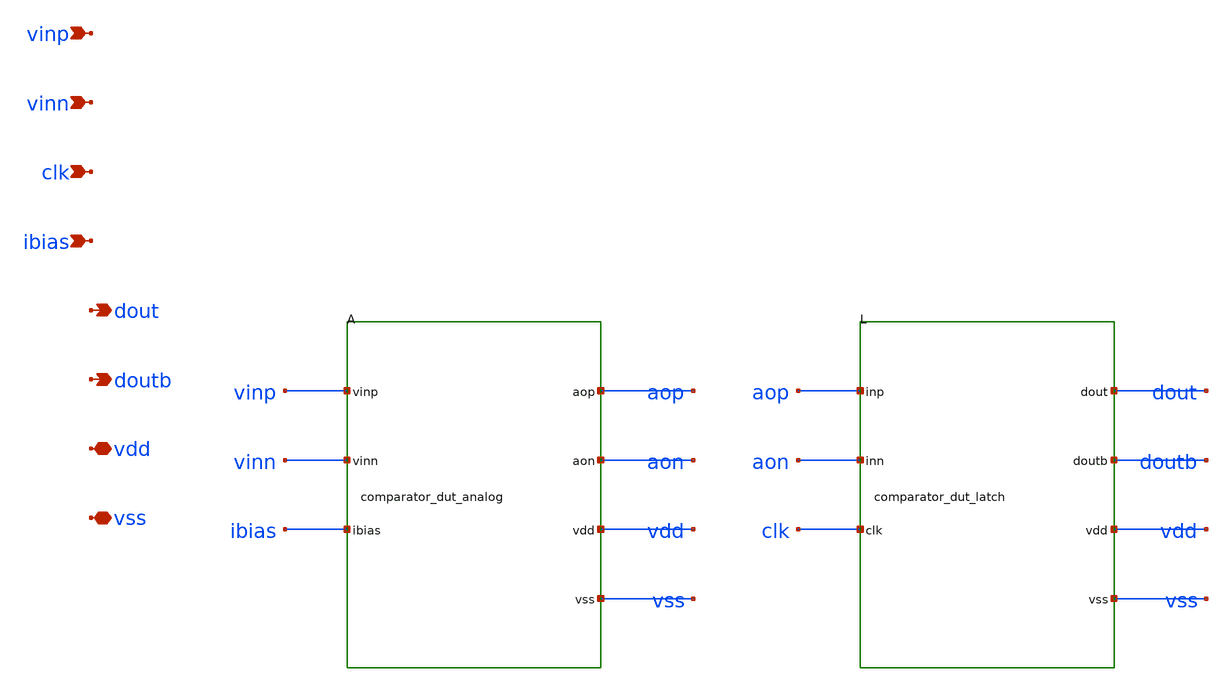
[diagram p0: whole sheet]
** sch_path: design/comparator_dut.sch
**.subckt comparator_dut vinp vinn clk ibias dout doutb vdd vss
*.ipin vinp
*.ipin vinn
*.ipin clk
*.ipin ibias
*.opin dout
*.opin doutb
*.iopin vdd
*.iopin vss
XA vinp vinn ibias aop aon vdd vss comparator_dut_analog
XL aop aon clk dout doutb vdd vss comparator_dut_latch
**.ends

* expanding   symbol:  comparator_dut_analog.sym # of pins=7
** sym_path: design/comparator_dut_analog.sym
** sch_path: design/comparator_dut_analog.sch
.subckt comparator_dut_analog vinp vinn ibias aop aon vdd vss

*.ipin vinp
*.ipin vinn
*.ipin ibias
*.opin aop
*.opin aon
*.iopin vdd
*.iopin vss
XMB ibias ibias vss vss nfet_03v3 L=4u W=5u nf=1 ad='int((nf+1)/2) * W/nf * 0.18u' as='int((nf+2)/2) * W/nf * 0.18u'
+ pd='2*int((nf+1)/2) * (W/nf + 0.18u)' ps='2*int((nf+2)/2) * (W/nf + 0.18u)' nrd='0.18u / W' nrs='0.18u / W'
+ sa=0 sb=0 sd=0 m=1
XMT atail ibias vss vss nfet_03v3 L=4u W=10u nf=1 ad='int((nf+1)/2) * W/nf * 0.18u' as='int((nf+2)/2) * W/nf * 0.18u'
+ pd='2*int((nf+1)/2) * (W/nf + 0.18u)' ps='2*int((nf+2)/2) * (W/nf + 0.18u)' nrd='0.18u / W' nrs='0.18u / W'
+ sa=0 sb=0 sd=0 m=1
XMIP aon vinp atail vss nfet_03v3 L=2u W=30u nf=1 ad='int((nf+1)/2) * W/nf * 0.18u' as='int((nf+2)/2) * W/nf * 0.18u'
+ pd='2*int((nf+1)/2) * (W/nf + 0.18u)' ps='2*int((nf+2)/2) * (W/nf + 0.18u)' nrd='0.18u / W' nrs='0.18u / W'
+ sa=0 sb=0 sd=0 m=1
XMIN aop vinn atail vss nfet_03v3 L=2u W=30u nf=1 ad='int((nf+1)/2) * W/nf * 0.18u' as='int((nf+2)/2) * W/nf * 0.18u'
+ pd='2*int((nf+1)/2) * (W/nf + 0.18u)' ps='2*int((nf+2)/2) * (W/nf + 0.18u)' nrd='0.18u / W' nrs='0.18u / W'
+ sa=0 sb=0 sd=0 m=1
XRN aon vdd vss ppolyf_u_1k r_width=1u r_length=120u m=1
XRP aop vdd vss ppolyf_u_1k r_width=1u r_length=120u m=1
.ends


* expanding   symbol:  comparator_dut_latch.sym # of pins=7
** sym_path: design/comparator_dut_latch.sym
** sch_path: design/comparator_dut_latch.sch
.subckt comparator_dut_latch inp inn clk dout doutb vdd vss

*.ipin inp
*.ipin inn
*.ipin clk
*.opin dout
*.opin doutb
*.iopin vdd
*.iopin vss
XMTL ltail clk vss vss nfet_03v3 L=0.5u W=16u nf=1 ad='int((nf+1)/2) * W/nf * 0.18u' as='int((nf+2)/2) * W/nf * 0.18u'
+ pd='2*int((nf+1)/2) * (W/nf + 0.18u)' ps='2*int((nf+2)/2) * (W/nf + 0.18u)' nrd='0.18u / W' nrs='0.18u / W'
+ sa=0 sb=0 sd=0 m=1
XM1 mn inp ltail vss nfet_03v3 L=0.5u W=8u nf=1 ad='int((nf+1)/2) * W/nf * 0.18u' as='int((nf+2)/2) * W/nf * 0.18u'
+ pd='2*int((nf+1)/2) * (W/nf + 0.18u)' ps='2*int((nf+2)/2) * (W/nf + 0.18u)' nrd='0.18u / W' nrs='0.18u / W'
+ sa=0 sb=0 sd=0 m=1
XM2 mp inn ltail vss nfet_03v3 L=0.5u W=8u nf=1 ad='int((nf+1)/2) * W/nf * 0.18u' as='int((nf+2)/2) * W/nf * 0.18u'
+ pd='2*int((nf+1)/2) * (W/nf + 0.18u)' ps='2*int((nf+2)/2) * (W/nf + 0.18u)' nrd='0.18u / W' nrs='0.18u / W'
+ sa=0 sb=0 sd=0 m=1
XM3 qn qp mn vss nfet_03v3 L=0.5u W=6u nf=1 ad='int((nf+1)/2) * W/nf * 0.18u' as='int((nf+2)/2) * W/nf * 0.18u'
+ pd='2*int((nf+1)/2) * (W/nf + 0.18u)' ps='2*int((nf+2)/2) * (W/nf + 0.18u)' nrd='0.18u / W' nrs='0.18u / W'
+ sa=0 sb=0 sd=0 m=1
XM4 qp qn mp vss nfet_03v3 L=0.5u W=6u nf=1 ad='int((nf+1)/2) * W/nf * 0.18u' as='int((nf+2)/2) * W/nf * 0.18u'
+ pd='2*int((nf+1)/2) * (W/nf + 0.18u)' ps='2*int((nf+2)/2) * (W/nf + 0.18u)' nrd='0.18u / W' nrs='0.18u / W'
+ sa=0 sb=0 sd=0 m=1
XM5 qn qp vdd vdd pfet_03v3 L=0.5u W=6u nf=1 ad='int((nf+1)/2) * W/nf * 0.18u' as='int((nf+2)/2) * W/nf * 0.18u'
+ pd='2*int((nf+1)/2) * (W/nf + 0.18u)' ps='2*int((nf+2)/2) * (W/nf + 0.18u)' nrd='0.18u / W' nrs='0.18u / W'
+ sa=0 sb=0 sd=0 m=1
XM6 qp qn vdd vdd pfet_03v3 L=0.5u W=6u nf=1 ad='int((nf+1)/2) * W/nf * 0.18u' as='int((nf+2)/2) * W/nf * 0.18u'
+ pd='2*int((nf+1)/2) * (W/nf + 0.18u)' ps='2*int((nf+2)/2) * (W/nf + 0.18u)' nrd='0.18u / W' nrs='0.18u / W'
+ sa=0 sb=0 sd=0 m=1
XM7 qn clk vdd vdd pfet_03v3 L=0.5u W=4u nf=1 ad='int((nf+1)/2) * W/nf * 0.18u' as='int((nf+2)/2) * W/nf * 0.18u'
+ pd='2*int((nf+1)/2) * (W/nf + 0.18u)' ps='2*int((nf+2)/2) * (W/nf + 0.18u)' nrd='0.18u / W' nrs='0.18u / W'
+ sa=0 sb=0 sd=0 m=1
XM8 qp clk vdd vdd pfet_03v3 L=0.5u W=4u nf=1 ad='int((nf+1)/2) * W/nf * 0.18u' as='int((nf+2)/2) * W/nf * 0.18u'
+ pd='2*int((nf+1)/2) * (W/nf + 0.18u)' ps='2*int((nf+2)/2) * (W/nf + 0.18u)' nrd='0.18u / W' nrs='0.18u / W'
+ sa=0 sb=0 sd=0 m=1
XM9 mn clk vdd vdd pfet_03v3 L=0.5u W=2u nf=1 ad='int((nf+1)/2) * W/nf * 0.18u' as='int((nf+2)/2) * W/nf * 0.18u'
+ pd='2*int((nf+1)/2) * (W/nf + 0.18u)' ps='2*int((nf+2)/2) * (W/nf + 0.18u)' nrd='0.18u / W' nrs='0.18u / W'
+ sa=0 sb=0 sd=0 m=1
XM10 mp clk vdd vdd pfet_03v3 L=0.5u W=2u nf=1 ad='int((nf+1)/2) * W/nf * 0.18u' as='int((nf+2)/2) * W/nf * 0.18u'
+ pd='2*int((nf+1)/2) * (W/nf + 0.18u)' ps='2*int((nf+2)/2) * (W/nf + 0.18u)' nrd='0.18u / W' nrs='0.18u / W'
+ sa=0 sb=0 sd=0 m=1
XIP1 sp qp vdd vdd pfet_03v3 L=0.5u W=5u nf=1 ad='int((nf+1)/2) * W/nf * 0.18u' as='int((nf+2)/2) * W/nf * 0.18u'
+ pd='2*int((nf+1)/2) * (W/nf + 0.18u)' ps='2*int((nf+2)/2) * (W/nf + 0.18u)' nrd='0.18u / W' nrs='0.18u / W'
+ sa=0 sb=0 sd=0 m=1
XIN1 sp qp vss vss nfet_03v3 L=0.5u W=2u nf=1 ad='int((nf+1)/2) * W/nf * 0.18u' as='int((nf+2)/2) * W/nf * 0.18u'
+ pd='2*int((nf+1)/2) * (W/nf + 0.18u)' ps='2*int((nf+2)/2) * (W/nf + 0.18u)' nrd='0.18u / W' nrs='0.18u / W'
+ sa=0 sb=0 sd=0 m=1
XIP2 sn qn vdd vdd pfet_03v3 L=0.5u W=5u nf=1 ad='int((nf+1)/2) * W/nf * 0.18u' as='int((nf+2)/2) * W/nf * 0.18u'
+ pd='2*int((nf+1)/2) * (W/nf + 0.18u)' ps='2*int((nf+2)/2) * (W/nf + 0.18u)' nrd='0.18u / W' nrs='0.18u / W'
+ sa=0 sb=0 sd=0 m=1
XIN2 sn qn vss vss nfet_03v3 L=0.5u W=2u nf=1 ad='int((nf+1)/2) * W/nf * 0.18u' as='int((nf+2)/2) * W/nf * 0.18u'
+ pd='2*int((nf+1)/2) * (W/nf + 0.18u)' ps='2*int((nf+2)/2) * (W/nf + 0.18u)' nrd='0.18u / W' nrs='0.18u / W'
+ sa=0 sb=0 sd=0 m=1
XA1P na sp vdd vdd pfet_03v3 L=0.5u W=10u nf=1 ad='int((nf+1)/2) * W/nf * 0.18u' as='int((nf+2)/2) * W/nf * 0.18u'
+ pd='2*int((nf+1)/2) * (W/nf + 0.18u)' ps='2*int((nf+2)/2) * (W/nf + 0.18u)' nrd='0.18u / W' nrs='0.18u / W'
+ sa=0 sb=0 sd=0 m=1
XA2P dout doutb na vdd pfet_03v3 L=0.5u W=10u nf=1 ad='int((nf+1)/2) * W/nf * 0.18u' as='int((nf+2)/2) * W/nf * 0.18u'
+ pd='2*int((nf+1)/2) * (W/nf + 0.18u)' ps='2*int((nf+2)/2) * (W/nf + 0.18u)' nrd='0.18u / W' nrs='0.18u / W'
+ sa=0 sb=0 sd=0 m=1
XA1N dout sp vss vss nfet_03v3 L=0.5u W=2u nf=1 ad='int((nf+1)/2) * W/nf * 0.18u' as='int((nf+2)/2) * W/nf * 0.18u'
+ pd='2*int((nf+1)/2) * (W/nf + 0.18u)' ps='2*int((nf+2)/2) * (W/nf + 0.18u)' nrd='0.18u / W' nrs='0.18u / W'
+ sa=0 sb=0 sd=0 m=1
XA2N dout doutb vss vss nfet_03v3 L=0.5u W=2u nf=1 ad='int((nf+1)/2) * W/nf * 0.18u' as='int((nf+2)/2) * W/nf * 0.18u'
+ pd='2*int((nf+1)/2) * (W/nf + 0.18u)' ps='2*int((nf+2)/2) * (W/nf + 0.18u)' nrd='0.18u / W' nrs='0.18u / W'
+ sa=0 sb=0 sd=0 m=1
XB1P nb sn vdd vdd pfet_03v3 L=0.5u W=10u nf=1 ad='int((nf+1)/2) * W/nf * 0.18u' as='int((nf+2)/2) * W/nf * 0.18u'
+ pd='2*int((nf+1)/2) * (W/nf + 0.18u)' ps='2*int((nf+2)/2) * (W/nf + 0.18u)' nrd='0.18u / W' nrs='0.18u / W'
+ sa=0 sb=0 sd=0 m=1
XB2P doutb dout nb vdd pfet_03v3 L=0.5u W=10u nf=1 ad='int((nf+1)/2) * W/nf * 0.18u' as='int((nf+2)/2) * W/nf * 0.18u'
+ pd='2*int((nf+1)/2) * (W/nf + 0.18u)' ps='2*int((nf+2)/2) * (W/nf + 0.18u)' nrd='0.18u / W' nrs='0.18u / W'
+ sa=0 sb=0 sd=0 m=1
XB1N doutb sn vss vss nfet_03v3 L=0.5u W=2u nf=1 ad='int((nf+1)/2) * W/nf * 0.18u' as='int((nf+2)/2) * W/nf * 0.18u'
+ pd='2*int((nf+1)/2) * (W/nf + 0.18u)' ps='2*int((nf+2)/2) * (W/nf + 0.18u)' nrd='0.18u / W' nrs='0.18u / W'
+ sa=0 sb=0 sd=0 m=1
XB2N doutb dout vss vss nfet_03v3 L=0.5u W=2u nf=1 ad='int((nf+1)/2) * W/nf * 0.18u' as='int((nf+2)/2) * W/nf * 0.18u'
+ pd='2*int((nf+1)/2) * (W/nf + 0.18u)' ps='2*int((nf+2)/2) * (W/nf + 0.18u)' nrd='0.18u / W' nrs='0.18u / W'
+ sa=0 sb=0 sd=0 m=1
.ends

.end
